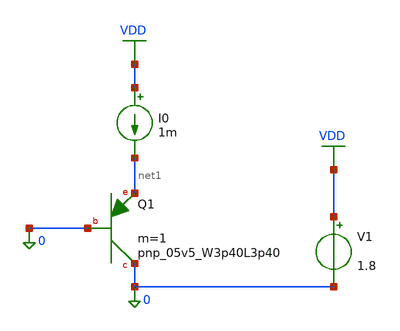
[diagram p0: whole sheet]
** sch_path: ctat.sch
**.subckt ctat
XQ1 0 0 net1 sky130_fd_pr__pnp_05v5_W3p40L3p40 m=1
I0 VDD net1 1m
V1 VDD 0 1.8
**** begin user architecture code


.lib /home/arunbalaji/open_pdks/sky130/sky130A/libs.tech/ngspice/sky130.lib.spice tt
.control
dc temp -40 80 1
run

* Plot V_BE
plot v(net1)

* Plot dV/dT
plot deriv(v(net1))

.endc

**** end user architecture code
**.ends
.GLOBAL VDD
.end
